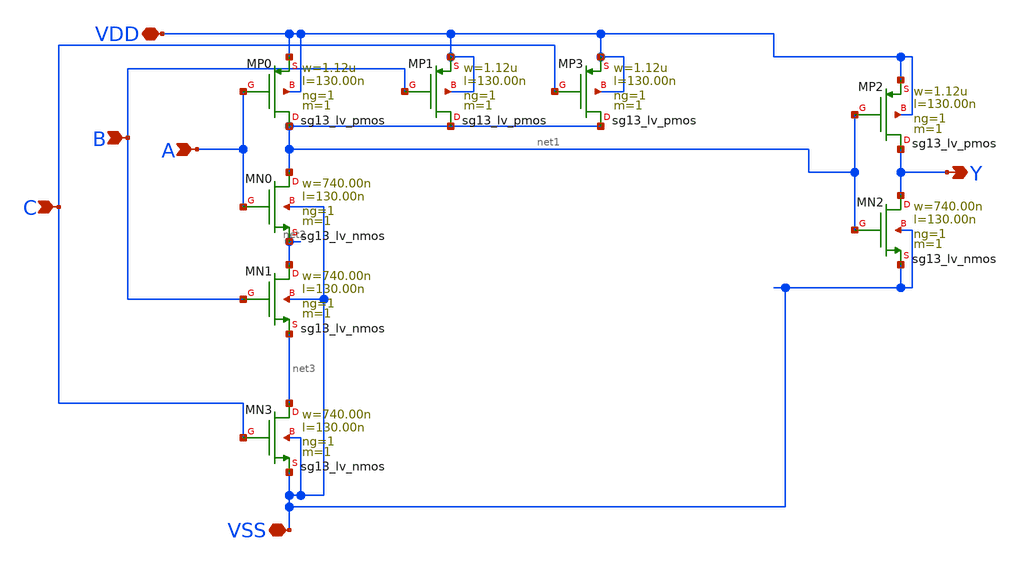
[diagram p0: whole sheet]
** sch_path: schematic/ANDtres.sch
**.subckt ANDtres A VDD VSS B Y C
*.ipin A
*.iopin VDD
*.iopin VSS
*.ipin B
*.opin Y
*.ipin C
XMN0 net1 A net2 VSS sg13_lv_nmos w=740.00n l=130.00n ng=1 m=1 mm_ok=1
XMP0 net1 A VDD VDD sg13_lv_pmos w=1.12u l=130.00n ng=1 m=1 mm_ok=1
XMP1 net1 B VDD VDD sg13_lv_pmos w=1.12u l=130.00n ng=1 m=1 mm_ok=1
XMN1 net2 B net3 VSS sg13_lv_nmos w=740.00n l=130.00n ng=1 m=1 mm_ok=1
XMN2 Y net1 VSS VSS sg13_lv_nmos w=740.00n l=130.00n ng=1 m=1 mm_ok=1
XMP2 Y net1 VDD VDD sg13_lv_pmos w=1.12u l=130.00n ng=1 m=1 mm_ok=1
XMP3 net1 C VDD VDD sg13_lv_pmos w=1.12u l=130.00n ng=1 m=1 mm_ok=1
XMN3 net3 C VSS VSS sg13_lv_nmos w=740.00n l=130.00n ng=1 m=1 mm_ok=1
**.ends
.end
